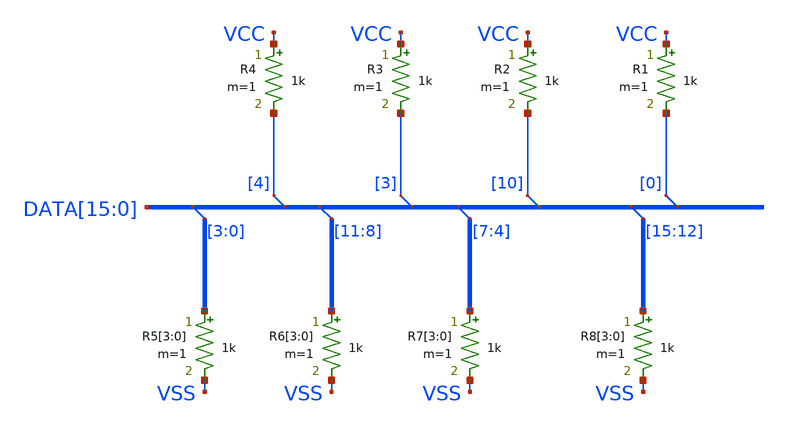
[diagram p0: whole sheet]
** sch_path: xschem_library/examples/test_bus_tap.sch
**.subckt test_bus_tap
* tap: DATA[15:0] --> DATA[3]
* tap: DATA[15:0] --> DATA[4]
* tap: DATA[15:0] --> DATA[7:4]
* tap: DATA[15:0] --> DATA[11:8]
* tap: DATA[15:0] --> DATA[3:0]
* tap: DATA[15:0] --> DATA[10]
* tap: DATA[15:0] --> DATA[0]
R1 VCC DATA[0] 1k m=1
R2 VCC DATA[10] 1k m=1
R3 VCC DATA[3] 1k m=1
R4 VCC DATA[4] 1k m=1
R5[3] DATA[3] VSS 1k m=1
R5[2] DATA[2] VSS 1k m=1
R5[1] DATA[1] VSS 1k m=1
R5[0] DATA[0] VSS 1k m=1
R6[3] DATA[11] VSS 1k m=1
R6[2] DATA[10] VSS 1k m=1
R6[1] DATA[9] VSS 1k m=1
R6[0] DATA[8] VSS 1k m=1
R7[3] DATA[7] VSS 1k m=1
R7[2] DATA[6] VSS 1k m=1
R7[1] DATA[5] VSS 1k m=1
R7[0] DATA[4] VSS 1k m=1
R8[3] DATA[15] VSS 1k m=1
R8[2] DATA[14] VSS 1k m=1
R8[1] DATA[13] VSS 1k m=1
R8[0] DATA[12] VSS 1k m=1
* tap: DATA[15:0] --> DATA[15:12]
**.ends
.end
